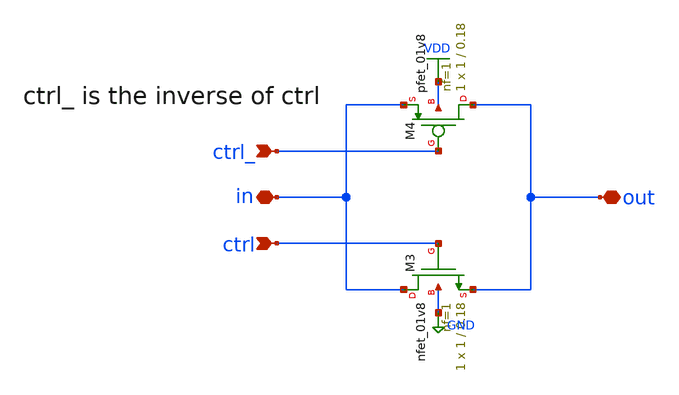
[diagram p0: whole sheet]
** sch_path: xschem/transmission_gate/transmission_gate.sch
**.subckt transmission_gate in out ctrl_ ctrl
*.iopin in
*.iopin out
*.ipin ctrl_
*.ipin ctrl
XM3 in ctrl out GND sky130_fd_pr__nfet_01v8 L=0.18 W=1 nf=1 ad='int((nf+1)/2) * W/nf * 0.29' as='int((nf+2)/2) * W/nf * 0.29'
+ pd='2*int((nf+1)/2) * (W/nf + 0.29)' ps='2*int((nf+2)/2) * (W/nf + 0.29)' nrd='0.29 / W' nrs='0.29 / W'
+ sa=0 sb=0 sd=0 mult=1 m=1
XM4 out ctrl_ in VDD sky130_fd_pr__pfet_01v8 L=0.18 W=1 nf=1 ad='int((nf+1)/2) * W/nf * 0.29' as='int((nf+2)/2) * W/nf * 0.29'
+ pd='2*int((nf+1)/2) * (W/nf + 0.29)' ps='2*int((nf+2)/2) * (W/nf + 0.29)' nrd='0.29 / W' nrs='0.29 / W'
+ sa=0 sb=0 sd=0 mult=1 m=1
**.ends
.GLOBAL GND
.GLOBAL VDD
.end
